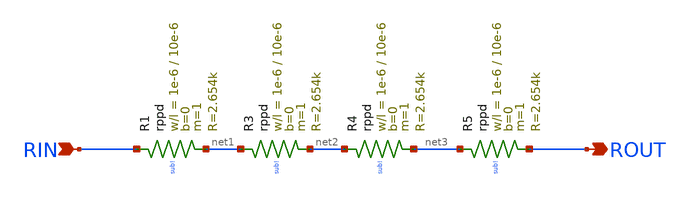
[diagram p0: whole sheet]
** sch_path: Cells/RES.sch
**.subckt RES RIN ROUT
*.ipin RIN
*.opin ROUT
XR1 RIN net1 sub! rppd w=1e-6 l=10e-6 m=1 b=0 mm_ok=1
XR3 net1 net2 sub! rppd w=1e-6 l=10e-6 m=1 b=0 mm_ok=1
XR4 net2 net3 sub! rppd w=1e-6 l=10e-6 m=1 b=0 mm_ok=1
XR5 net3 ROUT sub! rppd w=1e-6 l=10e-6 m=1 b=0 mm_ok=1
**.ends
.end
